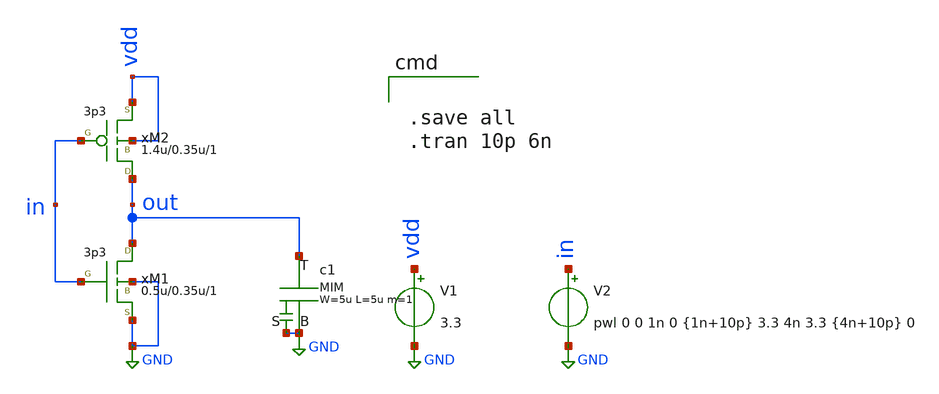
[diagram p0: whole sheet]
** sch_path: xschem/gen18_examples/inv.sch
**.subckt inv
V1 vdd GND 3.3
V2 in GND pwl 0 0 1n 0 {1n+10p} 3.3 4n 3.3 {4n+10p} 0
xc1 out GND GND cmim w=5u l=5u m=1
M1 out in GND GND nmos33 w=0.5u l=0.35u m=1 ad='2*0.5u *0.35u' as='2*0.5u *0.35u' pd='2*(0.5u +2*0.35u)'
+ ps='2*(0.5u +2*0.35u)'
M2 out in vdd vdd pmos33 w=1.4u l=0.35u m=1 ad='2*1.4u *0.35u' as='2*1.4u *0.35u' pd='2*(1.4u +2*0.35u)'
+ ps='2*(1.4u +2*0.35u)'
**** begin user architecture code

.save all
.tran 10p 6n

.include  [path_head [abs_sym_path gen18/gen18models.sym] 3]/mdl/gen18.inc
**** end user architecture code
**.ends
.GLOBAL GND
.end
